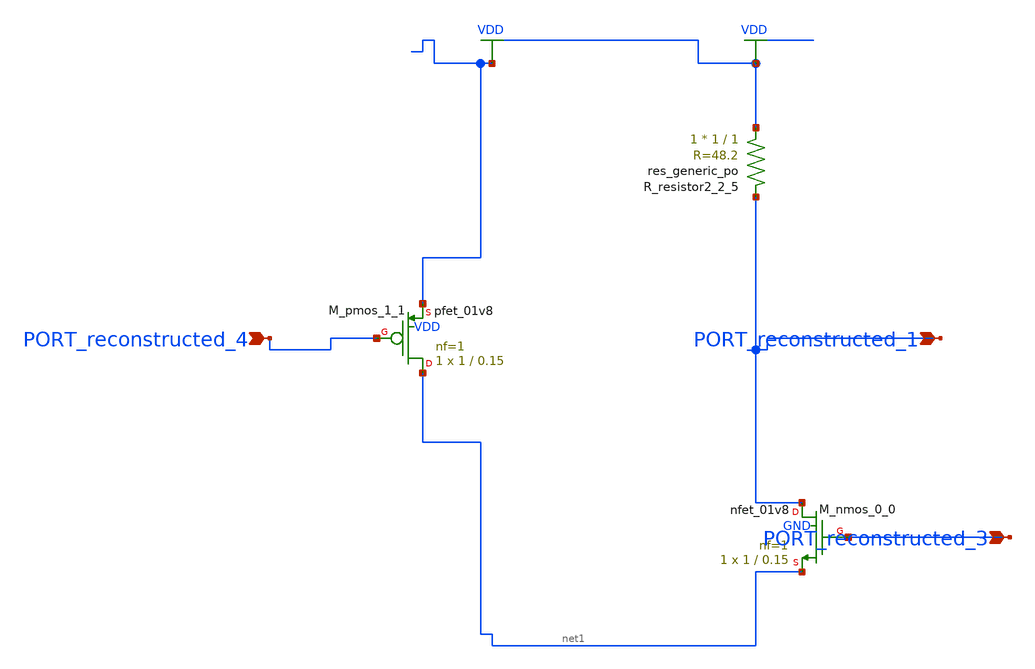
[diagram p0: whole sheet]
** sch_path: schematics/AMSNet/140.sch
**.subckt 140 PORT_reconstructed_3 PORT_reconstructed_1 PORT_reconstructed_4
*.ipin PORT_reconstructed_3
*.ipin PORT_reconstructed_1
*.ipin PORT_reconstructed_4
XM_nmos_0_0 PORT_reconstructed_1 PORT_reconstructed_3 net1 GND sky130_fd_pr__nfet_01v8 L=0.15 W=1 nf=1
+ ad='int((1 + 1)/2) * 1 / 1 * 0.29' as='int((1 + 2)/2) * 1 / 1 * 0.29' pd='2*int((1 + 1)/2) * (1 / 1 + 0.29)'
+ ps='2*int((1 + 2)/2) * (1 / 1 + 0.29)' nrd='0.29 / 1 ' nrs='0.29 / 1 ' sa=0 sb=0 sd=0 mult=1 m=1
XM_pmos_1_1 net1 PORT_reconstructed_4 VDD VDD sky130_fd_pr__pfet_01v8 L=0.15 W=1 nf=1 ad='int((1 + 1)/2) * 1 / 1 * 0.29'
+ as='int((1 + 2)/2) * 1 / 1 * 0.29' pd='2*int((1 + 1)/2) * (1 / 1 + 0.29)' ps='2*int((1 + 2)/2) * (1 / 1 + 0.29)'
+ nrd='0.29 / 1 ' nrs='0.29 / 1 ' sa=0 sb=0 sd=0 mult=1 m=1
XR_resistor2_2_5 VDD PORT_reconstructed_1 sky130_fd_pr__res_generic_po W=1 L=1 m=1
**.ends
.GLOBAL VDD
.end
